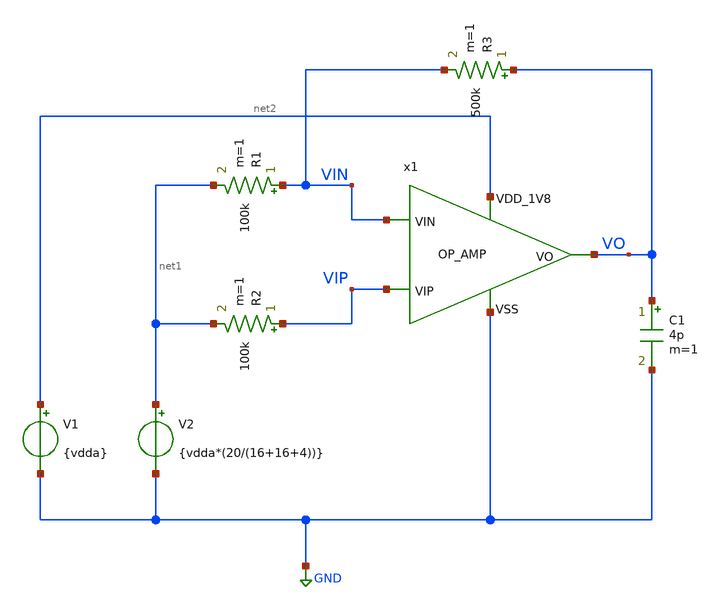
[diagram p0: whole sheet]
** sch_path: design/OP_AMP_SKY130NM/TB_OP_AMP.sch
**.subckt TB_OP_AMP
V2 net1 GND {vdda*(20/(16+16+4))}
R1 VIN net1 100k m=1
R2 VIP net1 100k m=1
C1 VO GND 4p m=1
R3 VO VIN 500k m=1
V1 net2 GND {vdda}
x1 net2 VO VIN VIP GND OP_AMP
**** begin user architecture code



* ngspice commands
.include corner.spi



**** end user architecture code
**.ends
.GLOBAL GND
.end
